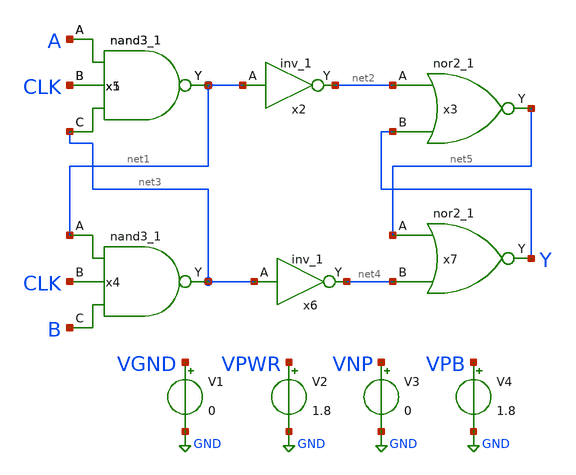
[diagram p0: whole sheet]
** sch_path: analog comparator/nand3-based_comp/schematics/comparator.sch
**.subckt comparator
x1 A CLK net3 VSS VSS VCC VCC net1 sky130_fd_sc_hd__nand3_1
x2 net1 VSS VSS VCC VCC net2 sky130_fd_sc_hd__inv_1
x3 net2 Y VSS VSS VCC VCC net5 sky130_fd_sc_hd__nor2_1
x4 net1 CLK B VSS VSS VCC VCC net3 sky130_fd_sc_hd__nand3_1
x5 A CLK net3 VSS VSS VCC VCC net1 sky130_fd_sc_hd__nand3_1
x6 net3 VSS VSS VCC VCC net4 sky130_fd_sc_hd__inv_1
x7 net5 net4 VSS VSS VCC VCC Y sky130_fd_sc_hd__nor2_1
V1 VGND GND 0
V2 VPWR GND 1.8
V3 VNP GND 0
V4 VPB GND 1.8
**.ends
.GLOBAL GND
.end
